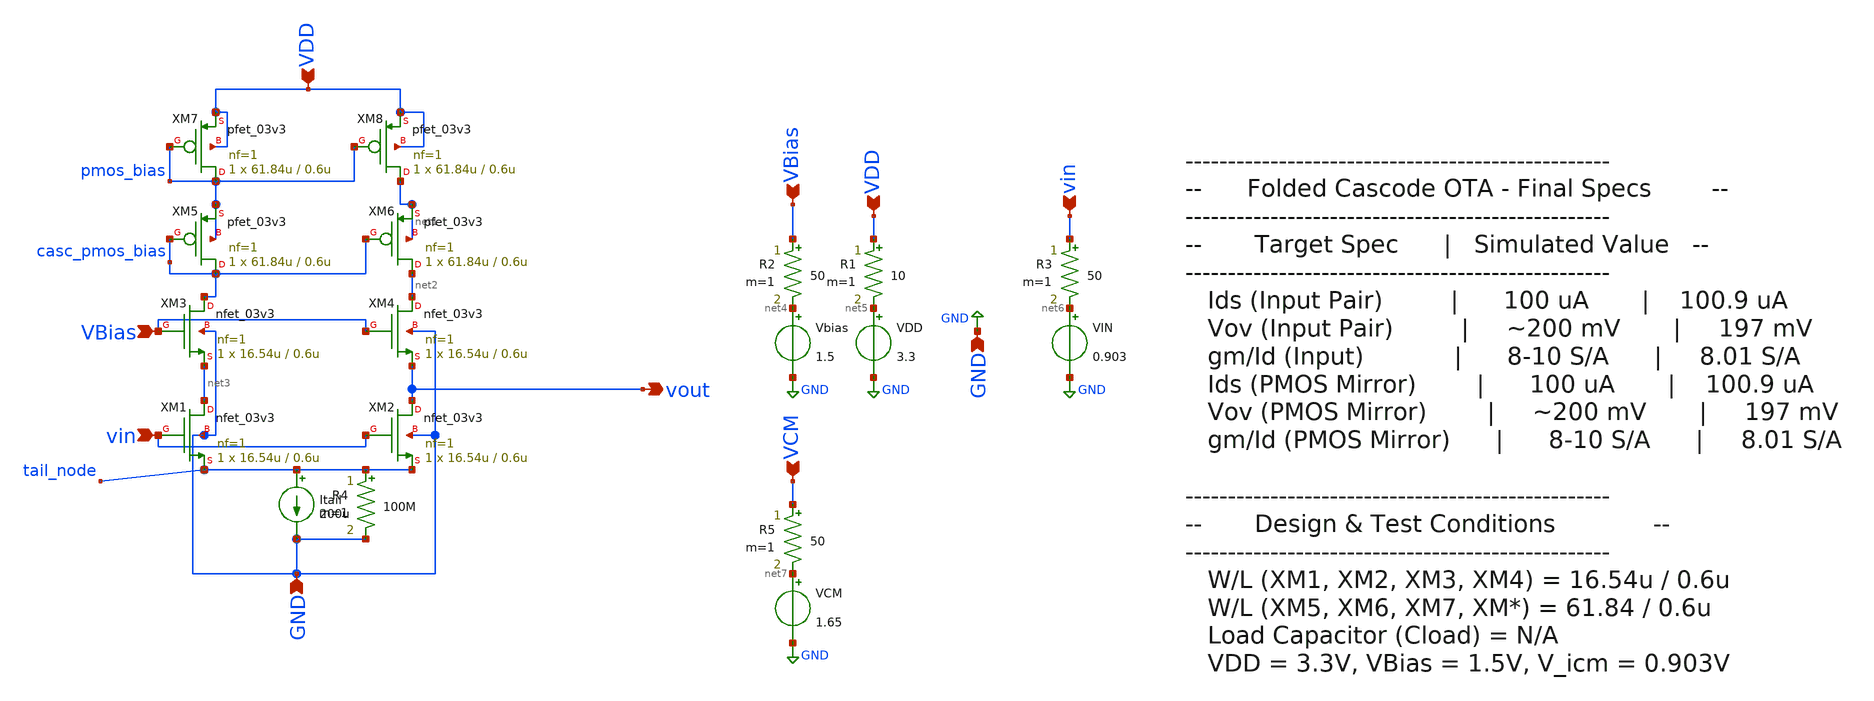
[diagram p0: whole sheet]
** sch_path: designs/athesh/folded_cascode.sch
**.subckt folded_cascode vin VBias VDD GND vout VBias VDD GND vin VCM
*.ipin vin
*.ipin VBias
*.ipin VDD
*.ipin GND
*.opin vout
*.ipin VBias
*.ipin VDD
*.ipin GND
*.ipin vin
*.ipin VCM
XM7 pmos_bias pmos_bias VDD VDD pfet_03v3 L=0.6u W=61.84u nf=1 ad='int((nf+1)/2) * W/nf * 0.18u' as='int((nf+2)/2) * W/nf * 0.18u'
+ pd='2*int((nf+1)/2) * (W/nf + 0.18u)' ps='2*int((nf+2)/2) * (W/nf + 0.18u)' nrd='0.18u / W' nrs='0.18u / W'
+ sa=0 sb=0 sd=0 m=1
XM8 net1 pmos_bias VDD VDD pfet_03v3 L=0.6u W=61.84u nf=1 ad='int((nf+1)/2) * W/nf * 0.18u' as='int((nf+2)/2) * W/nf * 0.18u'
+ pd='2*int((nf+1)/2) * (W/nf + 0.18u)' ps='2*int((nf+2)/2) * (W/nf + 0.18u)' nrd='0.18u / W' nrs='0.18u / W'
+ sa=0 sb=0 sd=0 m=1
XM5 casc_pmos_bias casc_pmos_bias pmos_bias pmos_bias pfet_03v3 L=0.6u W=61.84u nf=1 ad='int((nf+1)/2) * W/nf * 0.18u'
+ as='int((nf+2)/2) * W/nf * 0.18u' pd='2*int((nf+1)/2) * (W/nf + 0.18u)' ps='2*int((nf+2)/2) * (W/nf + 0.18u)'
+ nrd='0.18u / W' nrs='0.18u / W' sa=0 sb=0 sd=0 m=1
XM6 net2 casc_pmos_bias net1 net1 pfet_03v3 L=0.6u W=61.84u nf=1 ad='int((nf+1)/2) * W/nf * 0.18u' as='int((nf+2)/2) * W/nf * 0.18u'
+ pd='2*int((nf+1)/2) * (W/nf + 0.18u)' ps='2*int((nf+2)/2) * (W/nf + 0.18u)' nrd='0.18u / W' nrs='0.18u / W'
+ sa=0 sb=0 sd=0 m=1
XM3 casc_pmos_bias VBias net3 GND nfet_03v3 L=0.6u W=16.54u nf=1 ad='int((nf+1)/2) * W/nf * 0.18u' as='int((nf+2)/2) * W/nf * 0.18u'
+ pd='2*int((nf+1)/2) * (W/nf + 0.18u)' ps='2*int((nf+2)/2) * (W/nf + 0.18u)' nrd='0.18u / W' nrs='0.18u / W'
+ sa=0 sb=0 sd=0 m=1
XM4 net2 VBias vout GND nfet_03v3 L=0.6u W=16.54u nf=1 ad='int((nf+1)/2) * W/nf * 0.18u' as='int((nf+2)/2) * W/nf * 0.18u'
+ pd='2*int((nf+1)/2) * (W/nf + 0.18u)' ps='2*int((nf+2)/2) * (W/nf + 0.18u)' nrd='0.18u / W' nrs='0.18u / W'
+ sa=0 sb=0 sd=0 m=1
XM1 net3 vin tail_node GND nfet_03v3 L=0.6u W=16.54u nf=1 ad='int((nf+1)/2) * W/nf * 0.18u' as='int((nf+2)/2) * W/nf * 0.18u'
+ pd='2*int((nf+1)/2) * (W/nf + 0.18u)' ps='2*int((nf+2)/2) * (W/nf + 0.18u)' nrd='0.18u / W' nrs='0.18u / W'
+ sa=0 sb=0 sd=0 m=1
XM2 vout vin tail_node GND nfet_03v3 L=0.6u W=16.54u nf=1 ad='int((nf+1)/2) * W/nf * 0.18u' as='int((nf+2)/2) * W/nf * 0.18u'
+ pd='2*int((nf+1)/2) * (W/nf + 0.18u)' ps='2*int((nf+2)/2) * (W/nf + 0.18u)' nrd='0.18u / W' nrs='0.18u / W'
+ sa=0 sb=0 sd=0 m=1
Itail tail_node GND 200u
Vbias net4 GND 1.5
VDD net5 GND 3.3
VIN net6 GND 0.903
R1 VDD net5 10 m=1
R2 VBias net4 50 m=1
R3 vin net6 50 m=1
R4 tail_node GND 100M m=1
VCM net7 GND 1.65
R5 VCM net7 50 m=1
**** begin user architecture code



.control
save all


**Set Source
alter @VIN[AC] 1.0


**Simulations
*op
*ac dec 100 1 1G
*tran 0.1u 200u

write folded_cascode.raw
.endc



.include $::180MCU_MODELS/design.ngspice
.lib $::180MCU_MODELS/sm141064.ngspice typical

**** end user architecture code
**.ends
.GLOBAL GND
.end
